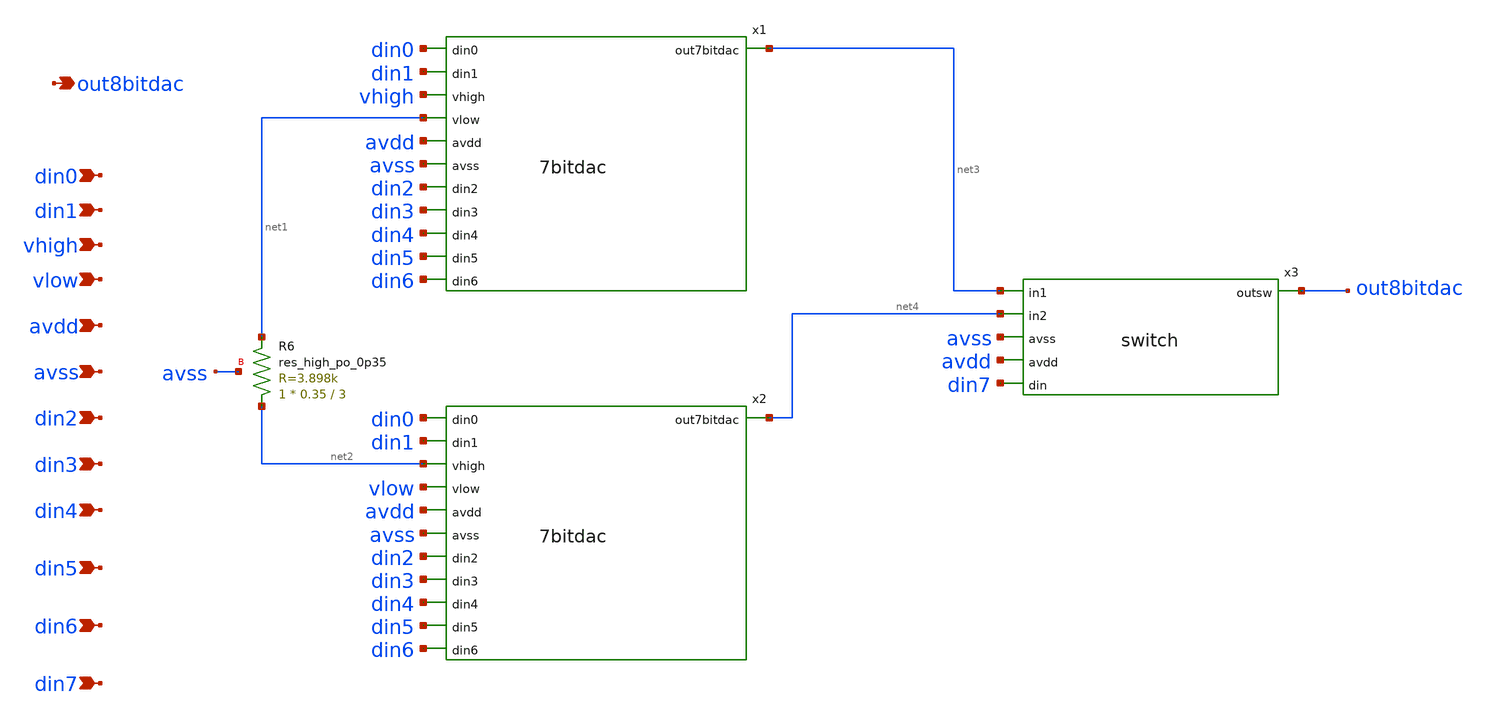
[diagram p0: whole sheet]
** sch_path: xschem/8bitdac.sch
**.subckt 8bitdac din0 din1 vhigh vlow avdd avss din2 din3 out8bitdac din4 din5 din6 din7
*.ipin din0
*.ipin din1
*.ipin vhigh
*.ipin vlow
*.ipin avdd
*.ipin avss
*.ipin din2
*.ipin din3
*.opin out8bitdac
*.ipin din4
*.ipin din5
*.ipin din6
*.ipin din7
x1 net3 din0 din1 vhigh net1 avdd avss din2 din3 din4 din5 din6 7bitdac
x2 net4 din0 din1 net2 vlow avdd avss din2 din3 din4 din5 din6 7bitdac
x3 out8bitdac net3 net4 avss avdd din7 switch
XR6 net2 net1 avss sky130_fd_pr__res_high_po_0p35 L=3 mult=1 m=1
**.ends
.end
